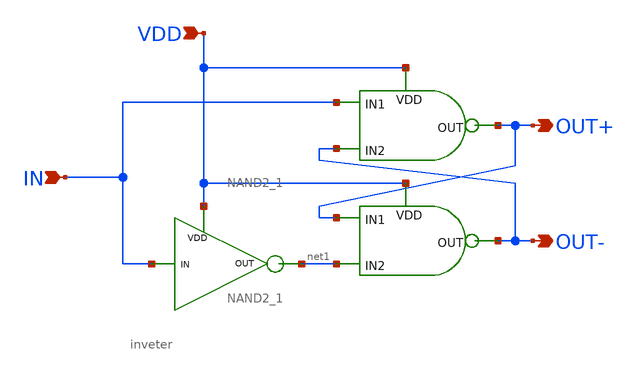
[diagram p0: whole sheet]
** sch_path: initial_notebooks_2023/Current-Steering DAC/latch1.sch
**.subckt latch1 VDD OUT+ IN OUT-
*.ipin VDD
*.opin OUT+
*.ipin IN
*.opin OUT-
x2 VDD net1 IN inveter
x1 VDD IN OUT+ OUT- NAND2_1
x3 VDD OUT+ OUT- net1 NAND2_1
**.ends
.end
